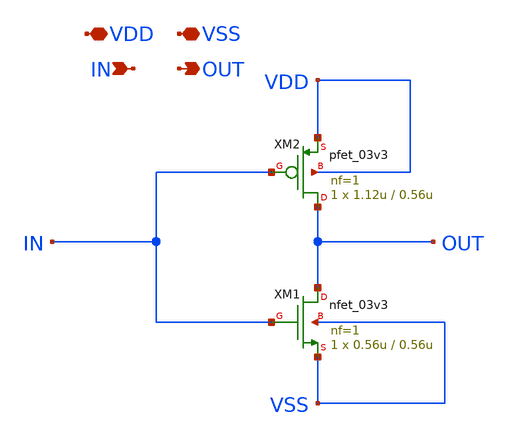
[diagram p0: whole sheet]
** sch_path: Clock_Generator_PAKISTAN_06/Xschem/GF_INV.sch
**.subckt GF_INV VDD VSS IN OUT
*.iopin VDD
*.iopin VSS
*.ipin IN
*.opin OUT
XM1 OUT IN VSS VSS nfet_03v3 L=0.56u W=0.56u nf=1 ad='int((nf+1)/2) * W/nf * 0.18u' as='int((nf+2)/2) * W/nf * 0.18u'
+ pd='2*int((nf+1)/2) * (W/nf + 0.18u)' ps='2*int((nf+2)/2) * (W/nf + 0.18u)' nrd='0.18u / W' nrs='0.18u / W'
+ sa=0 sb=0 sd=0 m=1
XM2 OUT IN VDD VDD pfet_03v3 L=0.56u W=1.12u nf=1 ad='int((nf+1)/2) * W/nf * 0.18u' as='int((nf+2)/2) * W/nf * 0.18u'
+ pd='2*int((nf+1)/2) * (W/nf + 0.18u)' ps='2*int((nf+2)/2) * (W/nf + 0.18u)' nrd='0.18u / W' nrs='0.18u / W'
+ sa=0 sb=0 sd=0 m=1
**.ends
.end
